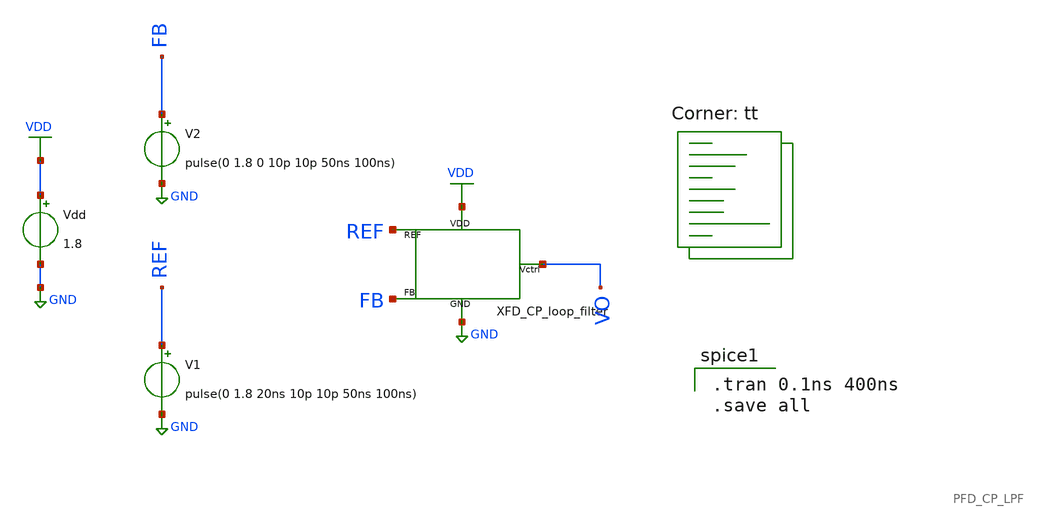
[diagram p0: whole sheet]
** sch_path: pll/pfd_cp_lf_lib/PFD_CP_LPF_tb/xschem/PFD_CP_LPF_tb.sch
**.subckt PFD_CP_LPF_tb
Vdd VDD GND 1.8
XFD_CP_loop_filter REF FB VO VDD GND PFD_CP_LPF
V1 REF GND pulse(0 1.8 20ns 10p 10p 50ns 100ns)
V2 FB GND pulse(0 1.8 0 10p 10p 50ns 100ns)
**** begin user architecture code
.lib $::SKYWATER_MODELS/sky130.lib.spice tt

.tran 0.1ns 400ns
.save all

**** end user architecture code
**.ends
.GLOBAL GND
.GLOBAL VDD
.end
